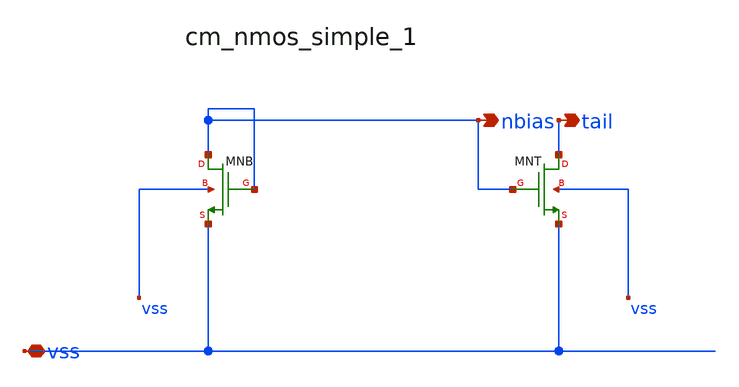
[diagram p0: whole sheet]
** sch_path: analog-db/raw/ldo_008_fer_mirror_ota/hier/blocks/cm_nmos_simple_1.sch
**.subckt cm_nmos_simple_1 vss nbias tail
*.iopin vss
*.opin nbias
*.opin tail
XMNB nbias nbias vss vss sg13_lv_nmos w=x_dut_xmnb_w l=x_dut_xmnb_l ng=1 m=x_dut_xmnb_m
XMNT tail nbias vss vss sg13_lv_nmos w=x_dut_xmnt_w l=x_dut_xmnt_l ng=1 m=x_dut_xmnt_m
**.ends
.end
